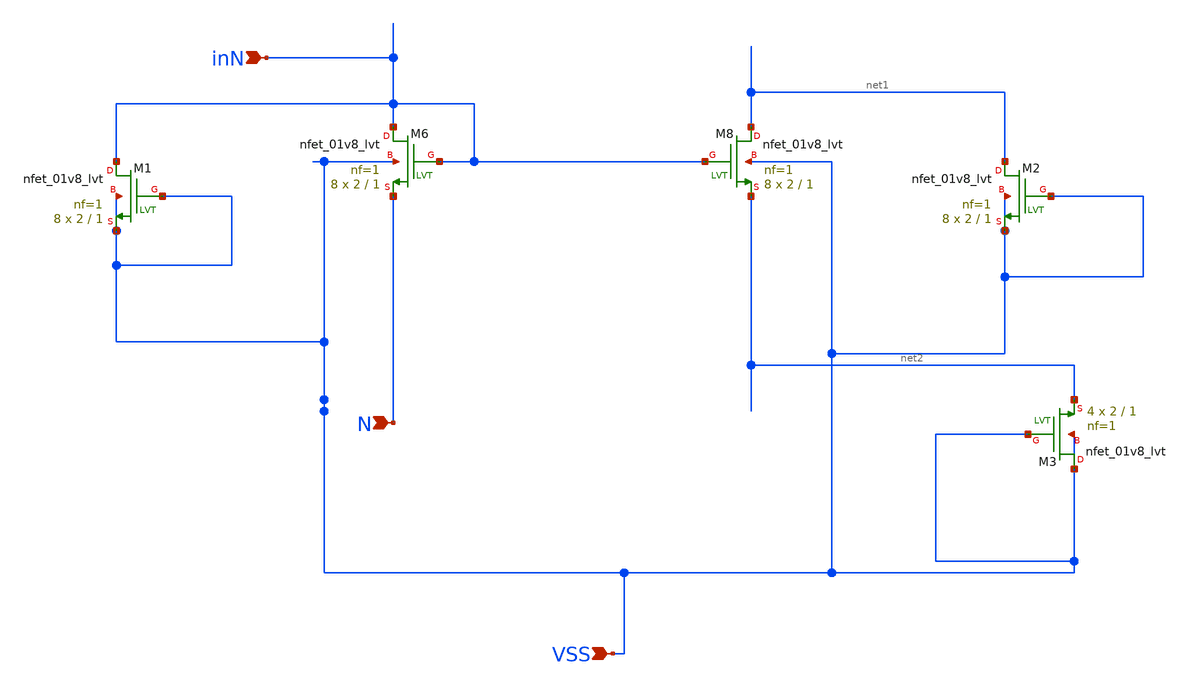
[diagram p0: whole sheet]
** sch_path: FTK/CM.sch
**.subckt CM inN VSS N
*.ipin inN
*.ipin VSS
*.ipin N
XM6 inN inN N VSS sky130_fd_pr__nfet_01v8_lvt L=1 W=2 nf=1 ad='int((1 + 1)/2) * 2 / 1 * 0.29' as='int((1 + 2)/2) * 2 / 1 * 0.29'
+ pd='2*int((1 + 1)/2) * (2 / 1 + 0.29)' ps='2*int((1 + 2)/2) * (2 / 1 + 0.29)' nrd='0.29 / 2 ' nrs='0.29 / 2 '
+ sa=0 sb=0 sd=0 mult=8 m=8
XM8 net1 inN net2 VSS sky130_fd_pr__nfet_01v8_lvt L=1 W=2 nf=1 ad='int((1 + 1)/2) * 2 / 1 * 0.29' as='int((1 + 2)/2) * 2 / 1 * 0.29'
+ pd='2*int((1 + 1)/2) * (2 / 1 + 0.29)' ps='2*int((1 + 2)/2) * (2 / 1 + 0.29)' nrd='0.29 / 2 ' nrs='0.29 / 2 '
+ sa=0 sb=0 sd=0 mult=8 m=8
XM1 inN VSS VSS VSS sky130_fd_pr__nfet_01v8_lvt L=1 W=2 nf=1 ad='int((1 + 1)/2) * 2 / 1 * 0.29' as='int((1 + 2)/2) * 2 / 1 * 0.29'
+ pd='2*int((1 + 1)/2) * (2 / 1 + 0.29)' ps='2*int((1 + 2)/2) * (2 / 1 + 0.29)' nrd='0.29 / 2 ' nrs='0.29 / 2 '
+ sa=0 sb=0 sd=0 mult=8 m=8
XM2 net1 VSS VSS VSS sky130_fd_pr__nfet_01v8_lvt L=1 W=2 nf=1 ad='int((1 + 1)/2) * 2 / 1 * 0.29' as='int((1 + 2)/2) * 2 / 1 * 0.29'
+ pd='2*int((1 + 1)/2) * (2 / 1 + 0.29)' ps='2*int((1 + 2)/2) * (2 / 1 + 0.29)' nrd='0.29 / 2 ' nrs='0.29 / 2 '
+ sa=0 sb=0 sd=0 mult=8 m=8
XM3 VSS VSS net2 VSS sky130_fd_pr__nfet_01v8_lvt L=1 W=2 nf=1 ad='int((1 + 1)/2) * 2 / 1 * 0.29' as='int((1 + 2)/2) * 2 / 1 * 0.29'
+ pd='2*int((1 + 1)/2) * (2 / 1 + 0.29)' ps='2*int((1 + 2)/2) * (2 / 1 + 0.29)' nrd='0.29 / 2 ' nrs='0.29 / 2 '
+ sa=0 sb=0 sd=0 mult=4 m=4
**.ends
.end
